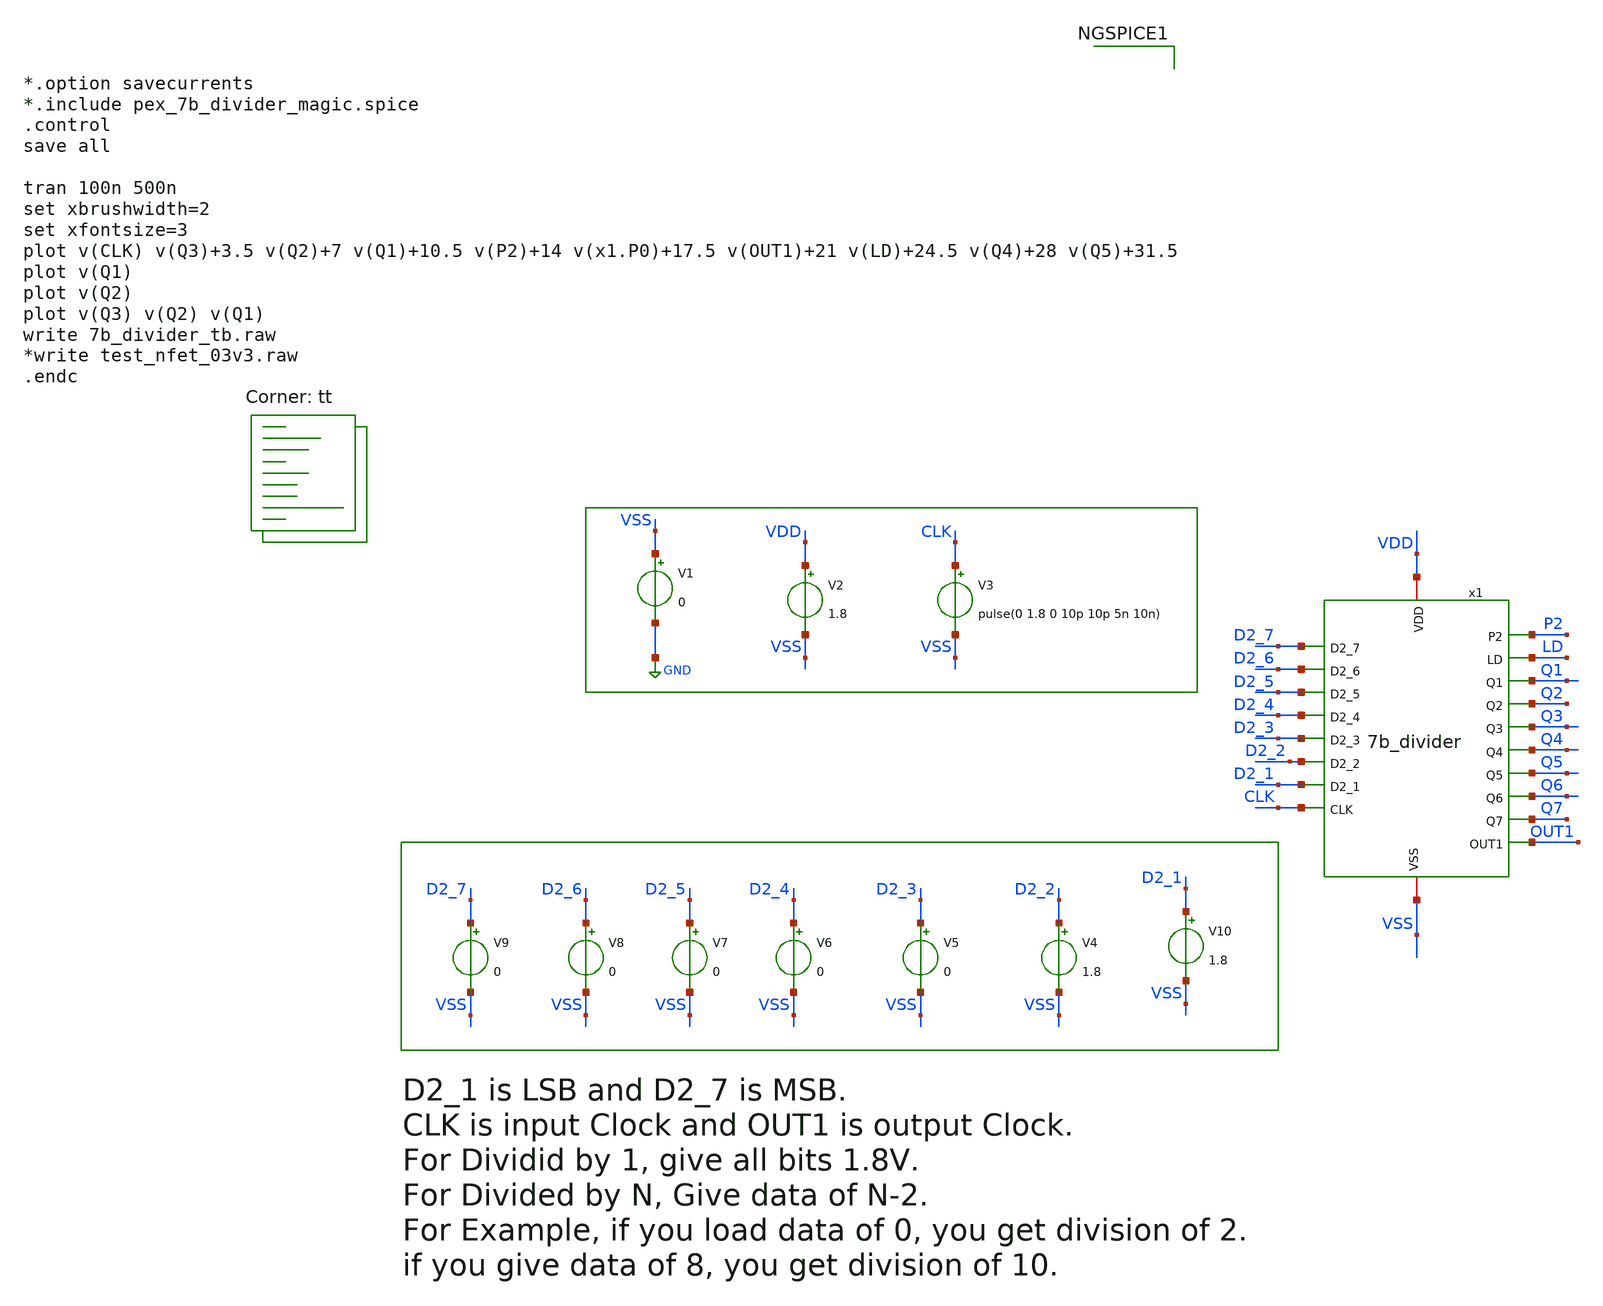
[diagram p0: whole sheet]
** sch_path: Xschem/PLL_TOP_Schematics/7b_divider_tb.sch
**.subckt 7b_divider_tb
V1 VSS GND 0
V2 VDD VSS 1.8
V3 CLK VSS pulse(0 1.8 0 10p 10p 5n 10n)
x1 VDD LD D2_7 Q1 D2_6 Q2 D2_5 D2_4 Q3 Q4 D2_3 D2_2 Q5 D2_1 Q6 Q7 CLK VSS OUT1 P2 7b_divider
V10 D2_1 VSS 1.8
V4 D2_2 VSS 1.8
V5 D2_3 VSS 0
V6 D2_4 VSS 0
V7 D2_5 VSS 0
V8 D2_6 VSS 0
V9 D2_7 VSS 0
**** begin user architecture code


*.option savecurrents
*.include pex_7b_divider_magic.spice
.control
save all

tran 100n 500n
set xbrushwidth=2
set xfontsize=3
plot v(CLK) v(Q3)+3.5 v(Q2)+7 v(Q1)+10.5 v(P2)+14 v(x1.P0)+17.5 v(OUT1)+21 v(LD)+24.5 v(Q4)+28
+ v(Q5)+31.5
plot v(Q1)
plot v(Q2)
plot v(Q3) v(Q2) v(Q1)
write 7b_divider_tb.raw
*write test_nfet_03v3.raw
.endc


.lib $::SKYWATER_MODELS/sky130.lib.spice tt
**** end user architecture code
**.ends
.GLOBAL GND
.end
